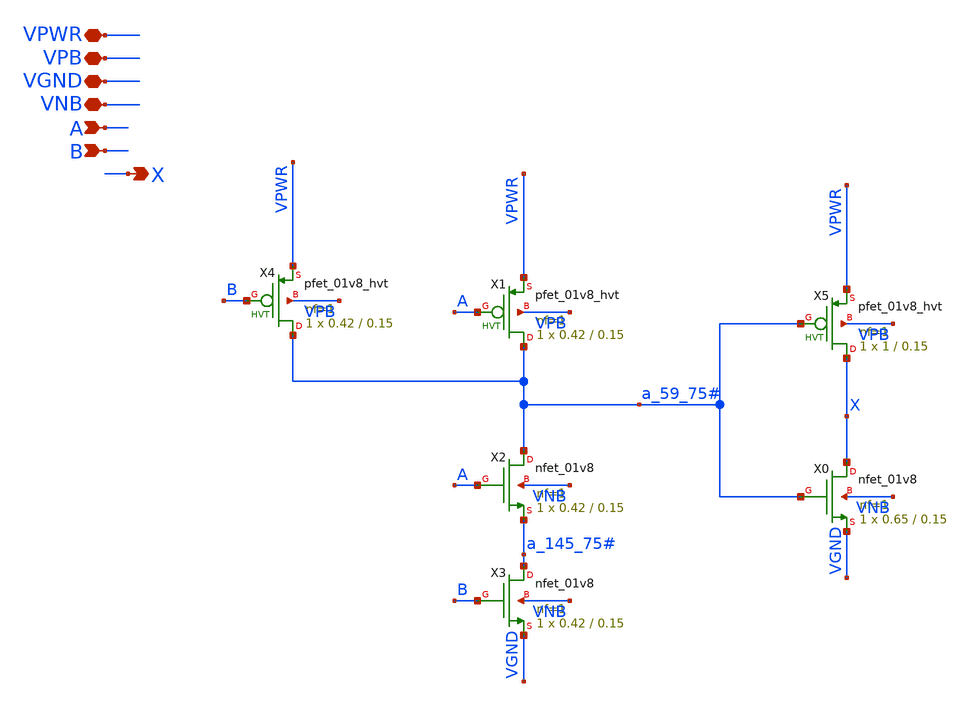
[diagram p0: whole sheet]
** sch_path: analog/klayout/production/final_merge_20260923/testbenches/cace/analog/xschem/sky130_fd_sc_hd__and2_1.sch
**.subckt sky130_fd_sc_hd__and2_1 A X VNB VPB VPWR B VGND
*.ipin A
*.opin X
*.iopin VNB
*.iopin VPB
*.iopin VPWR
*.ipin B
*.iopin VGND
XX0 X a_59_75# VGND VNB sky130_fd_pr__nfet_01v8 L=0.15 W=0.65 nf=1 ad='int((1 + 1)/2) * 0.65 / 1 * 0.29'
+ as='int((1 + 2)/2) * 0.65 / 1 * 0.29' pd='2*int((1 + 1)/2) * (0.65 / 1 + 0.29)' ps='2*int((1 + 2)/2) * (0.65 / 1 + 0.29)'
+ nrd='0.29 / 0.65 ' nrs='0.29 / 0.65 ' sa=0 sb=0 sd=0 mult=1 m=1
XX4 a_59_75# B VPWR VPB sky130_fd_pr__pfet_01v8_hvt L=0.15 W=0.42 nf=1 ad='int((1 + 1)/2) * 0.42 / 1 * 0.29'
+ as='int((1 + 2)/2) * 0.42 / 1 * 0.29' pd='2*int((1 + 1)/2) * (0.42 / 1 + 0.29)' ps='2*int((1 + 2)/2) * (0.42 / 1 + 0.29)'
+ nrd='0.29 / 0.42 ' nrs='0.29 / 0.42 ' sa=0 sb=0 sd=0 mult=1 m=1
XX1 a_59_75# A VPWR VPB sky130_fd_pr__pfet_01v8_hvt L=0.15 W=0.42 nf=1 ad='int((1 + 1)/2) * 0.42 / 1 * 0.29'
+ as='int((1 + 2)/2) * 0.42 / 1 * 0.29' pd='2*int((1 + 1)/2) * (0.42 / 1 + 0.29)' ps='2*int((1 + 2)/2) * (0.42 / 1 + 0.29)'
+ nrd='0.29 / 0.42 ' nrs='0.29 / 0.42 ' sa=0 sb=0 sd=0 mult=1 m=1
XX5 X a_59_75# VPWR VPB sky130_fd_pr__pfet_01v8_hvt L=0.15 W=1 nf=1 ad='int((1 + 1)/2) * 1 / 1 * 0.29'
+ as='int((1 + 2)/2) * 1 / 1 * 0.29' pd='2*int((1 + 1)/2) * (1 / 1 + 0.29)' ps='2*int((1 + 2)/2) * (1 / 1 + 0.29)'
+ nrd='0.29 / 1 ' nrs='0.29 / 1 ' sa=0 sb=0 sd=0 mult=1 m=1
XX2 a_59_75# A a_145_75# VNB sky130_fd_pr__nfet_01v8 L=0.15 W=0.42 nf=1 ad='int((1 + 1)/2) * 0.42 / 1 * 0.29'
+ as='int((1 + 2)/2) * 0.42 / 1 * 0.29' pd='2*int((1 + 1)/2) * (0.42 / 1 + 0.29)' ps='2*int((1 + 2)/2) * (0.42 / 1 + 0.29)'
+ nrd='0.29 / 0.42 ' nrs='0.29 / 0.42 ' sa=0 sb=0 sd=0 mult=1 m=1
XX3 a_145_75# B VGND VNB sky130_fd_pr__nfet_01v8 L=0.15 W=0.42 nf=1 ad='int((1 + 1)/2) * 0.42 / 1 * 0.29'
+ as='int((1 + 2)/2) * 0.42 / 1 * 0.29' pd='2*int((1 + 1)/2) * (0.42 / 1 + 0.29)' ps='2*int((1 + 2)/2) * (0.42 / 1 + 0.29)'
+ nrd='0.29 / 0.42 ' nrs='0.29 / 0.42 ' sa=0 sb=0 sd=0 mult=1 m=1
**.ends
.end
